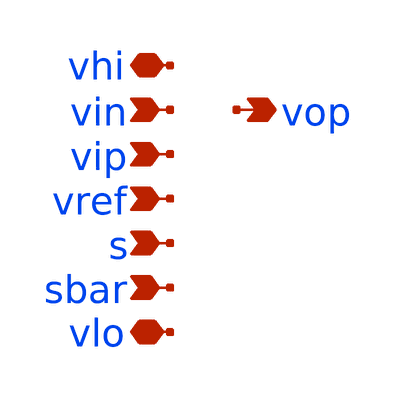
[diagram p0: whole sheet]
** sch_path: xschem/dut_opa_top_pex.sch
**.subckt dut_opa_top_pex vip vin vop vhi vlo vref s sbar
*.ipin vip
*.ipin vin
*.opin vop
*.iopin vhi
*.iopin vlo
*.ipin vref
*.ipin s
*.ipin sbar
**** begin user architecture code

* NGSPICE file created from cmota_1_flat.ext - technology: sky130A

.subckt cmota_gb_rp_gp VHI VLO VREF VIP VIN VOP S SBAR


X0 VOP a_19556_n5512# VHI VHI sky130_fd_pr__pfet_01v8 ad=0p pd=0u as=0p ps=0u w=1e+07u l=300000u
X1 a_19201_n6600# VIN a_18258_n5512# VLO sky130_fd_pr__nfet_01v8_lvt ad=0p pd=0u as=0p ps=0u
+ w=2.5e+06u l=150000u
X2 a_18258_n5512# VIN a_19201_n6600# VLO sky130_fd_pr__nfet_01v8_lvt ad=0p pd=0u as=0p ps=0u
+ w=2.5e+06u l=150000u
X3 VLO VLO VLO VLO sky130_fd_pr__nfet_01v8 ad=0p pd=0u as=0p ps=0u w=1e+07u l=300000u
X4 a_18021_n8012# a_22692_n6680# VLO sky130_fd_pr__res_high_po w=690000u l=5.83e+06u
D0 VLO VIP sky130_fd_pr__diode_pw2nd_05v5 pj=2.64e+06 area=4.347e+11
X5 a_19201_n6600# a_16650_n8544# VLO VLO sky130_fd_pr__nfet_01v8 ad=0p pd=0u as=0p ps=0u w=1e+07u
+ l=2e+06u
X6 VLO a_18021_n8012# VOP VLO sky130_fd_pr__nfet_01v8 ad=0p pd=0u as=0p ps=0u w=1e+07u l=300000u
X7 VHI VLO sky130_fd_pr__cap_mim_m3_1 l=3.1e+07u w=1.3e+07u
X8 VLO a_18021_n8012# a_18021_n8012# VLO sky130_fd_pr__nfet_01v8 ad=0p pd=0u as=0p ps=0u w=1e+07u
+ l=300000u
X9 a_16606_n9004# S a_16650_n8544# VLO sky130_fd_pr__nfet_01v8 ad=0p pd=0u as=0p ps=0u w=2.5e+06u
+ l=150000u
D1 VREF VHI sky130_fd_pr__diode_pd2nw_05v5 pj=3.34e+06 area=6.552e+11
X10 VLO a_16650_n8544# sky130_fd_pr__cap_mim_m3_1 l=2.7e+07u w=5.5e+06u
X11 VLO VLO VLO VLO sky130_fd_pr__nfet_01v8 ad=0p pd=0u as=0p ps=0u w=1e+07u l=300000u
X12 a_19619_n5415# a_19556_n5512# VHI VHI sky130_fd_pr__pfet_01v8 ad=0p pd=0u as=0p ps=0u w=1e+07u
+ l=300000u
X13 VHI a_19556_n5512# a_19619_n5415# VHI sky130_fd_pr__pfet_01v8 ad=0p pd=0u as=0p ps=0u w=1e+07u
+ l=300000u
X14 VHI a_18258_n5512# a_19556_n5512# VHI sky130_fd_pr__pfet_01v8 ad=0p pd=0u as=0p ps=0u w=1e+07u
+ l=300000u
X15 VOP a_19556_n5512# VHI VHI sky130_fd_pr__pfet_01v8 ad=0p pd=0u as=0p ps=0u w=1e+07u l=300000u
X16 a_19556_n5512# VIP a_19201_n6600# VLO sky130_fd_pr__nfet_01v8_lvt ad=0p pd=0u as=0p ps=0u
+ w=2.5e+06u l=150000u
D2 VIP VHI sky130_fd_pr__diode_pd2nw_05v5 pj=3.34e+06 area=6.552e+11
X17 a_18258_n5512# a_19556_n5512# VHI VHI sky130_fd_pr__pfet_01v8 ad=0p pd=0u as=0p ps=0u w=1e+07u
+ l=300000u
X18 a_20327_n5415# a_18258_n5512# VHI VHI sky130_fd_pr__pfet_01v8 ad=0p pd=0u as=0p ps=0u w=1e+07u
+ l=300000u
X19 a_19201_n6600# VIP a_19556_n5512# VLO sky130_fd_pr__nfet_01v8_lvt ad=0p pd=0u as=0p ps=0u
+ w=2.5e+06u l=150000u
X20 VHI a_18258_n5512# a_20327_n5415# VHI sky130_fd_pr__pfet_01v8 ad=0p pd=0u as=0p ps=0u w=1e+07u
+ l=300000u
X21 a_18021_n8012# a_18258_n5512# VHI VHI sky130_fd_pr__pfet_01v8 ad=0p pd=0u as=0p ps=0u w=1e+07u
+ l=300000u
X22 a_18258_n5512# VIN a_19201_n6600# VLO sky130_fd_pr__nfet_01v8_lvt ad=0p pd=0u as=0p ps=0u
+ w=2.5e+06u l=150000u
X23 a_19201_n6600# a_16650_n8544# VLO VLO sky130_fd_pr__nfet_01v8 ad=0p pd=0u as=0p ps=0u w=1e+07u
+ l=2e+06u
X24 VHI a_18258_n5512# a_18021_n8012# VHI sky130_fd_pr__pfet_01v8 ad=0p pd=0u as=0p ps=0u w=1e+07u
+ l=300000u
X25 a_18021_n8012# a_18258_n5512# VHI VHI sky130_fd_pr__pfet_01v8 ad=0p pd=0u as=0p ps=0u w=1e+07u
+ l=300000u
X26 a_19201_n6600# VIN a_18258_n5512# VLO sky130_fd_pr__nfet_01v8_lvt ad=0p pd=0u as=0p ps=0u
+ w=2.5e+06u l=150000u
X27 a_19201_n6600# VIP a_19556_n5512# VLO sky130_fd_pr__nfet_01v8_lvt ad=0p pd=0u as=0p ps=0u
+ w=2.5e+06u l=150000u
X28 VLO a_16650_n8544# a_19201_n6600# VLO sky130_fd_pr__nfet_01v8 ad=0p pd=0u as=0p ps=0u w=1e+07u
+ l=2e+06u
X29 a_16650_n8544# VLO sky130_fd_pr__cap_mim_m3_2 l=2.7e+07u w=5.5e+06u
X30 VLO VHI sky130_fd_pr__cap_mim_m3_2 l=3.1e+07u w=1.3e+07u
X31 VLO VLO VLO VLO sky130_fd_pr__nfet_01v8_lvt ad=0p pd=0u as=0p ps=0u w=2.5e+06u l=150000u
X32 VLO VLO a_19201_n6600# VLO sky130_fd_pr__nfet_01v8_lvt ad=0p pd=0u as=0p ps=0u w=2.5e+06u
+ l=150000u
X33 VLO VLO VLO VLO sky130_fd_pr__nfet_01v8_lvt ad=0p pd=0u as=0p ps=0u w=2.5e+06u l=150000u
X34 VOP a_22692_n6680# sky130_fd_pr__cap_mim_m3_1 l=1.32e+07u w=3.7e+06u
X35 a_19201_n6600# VIN a_18258_n5512# VLO sky130_fd_pr__nfet_01v8_lvt ad=0p pd=0u as=0p ps=0u
+ w=2.5e+06u l=150000u
X36 a_16650_n8544# S a_16606_n9004# VLO sky130_fd_pr__nfet_01v8 ad=0p pd=0u as=0p ps=0u w=2.5e+06u
+ l=150000u
X37 VREF a_16606_n9004# VLO sky130_fd_pr__res_xhigh_po w=350000u l=1.49e+06u
X38 VLO VLO VLO VLO sky130_fd_pr__nfet_01v8 ad=0p pd=0u as=0p ps=0u w=1e+07u l=300000u
X39 VOP a_18021_n8012# VLO VLO sky130_fd_pr__nfet_01v8 ad=0p pd=0u as=0p ps=0u w=1e+07u l=300000u
X40 VHI a_19556_n5512# VOP VHI sky130_fd_pr__pfet_01v8 ad=0p pd=0u as=0p ps=0u w=1e+07u l=300000u
X41 a_19201_n6600# VLO VLO VLO sky130_fd_pr__nfet_01v8_lvt ad=0p pd=0u as=0p ps=0u w=2.5e+06u
+ l=150000u
X42 a_16606_n9004# SBAR VLO VLO sky130_fd_pr__nfet_01v8 ad=0p pd=0u as=0p ps=0u w=2.5e+06u l=150000u
X43 VLO a_18021_n8012# VOP VLO sky130_fd_pr__nfet_01v8 ad=0p pd=0u as=0p ps=0u w=1e+07u l=300000u
X44 a_18258_n5512# a_18258_n5512# VHI VHI sky130_fd_pr__pfet_01v8 ad=0p pd=0u as=0p ps=0u w=1e+07u
+ l=300000u
X45 VOP a_19556_n5512# VHI VHI sky130_fd_pr__pfet_01v8 ad=0p pd=0u as=0p ps=0u w=1e+07u l=300000u
X46 a_18258_n5512# VIN a_19201_n6600# VLO sky130_fd_pr__nfet_01v8_lvt ad=0p pd=0u as=0p ps=0u
+ w=2.5e+06u l=150000u
D3 VLO VIN sky130_fd_pr__diode_pw2nd_05v5 pj=2.64e+06 area=4.347e+11
X47 VHI a_19556_n5512# VOP VHI sky130_fd_pr__pfet_01v8 ad=0p pd=0u as=0p ps=0u w=1e+07u l=300000u
X48 VOP a_19556_n5512# VHI VHI sky130_fd_pr__pfet_01v8 ad=0p pd=0u as=0p ps=0u w=1e+07u l=300000u
X49 a_22692_n6680# VOP sky130_fd_pr__cap_mim_m3_2 l=1.32e+07u w=3.7e+06u
X50 a_18021_n8012# VHI VHI VHI sky130_fd_pr__pfet_01v8 ad=0p pd=0u as=0p ps=0u w=1e+07u l=300000u
X51 VHI a_18258_n5512# a_18021_n8012# VHI sky130_fd_pr__pfet_01v8 ad=0p pd=0u as=0p ps=0u w=1e+07u
+ l=300000u
X52 VHI a_19556_n5512# a_18258_n5512# VHI sky130_fd_pr__pfet_01v8 ad=0p pd=0u as=0p ps=0u w=1e+07u
+ l=300000u
X53 a_19556_n5512# a_19556_n5512# VHI VHI sky130_fd_pr__pfet_01v8 ad=0p pd=0u as=0p ps=0u w=1e+07u
+ l=300000u
D4 VIN VHI sky130_fd_pr__diode_pd2nw_05v5 pj=3.34e+06 area=6.552e+11
X54 VHI a_18258_n5512# a_18021_n8012# VHI sky130_fd_pr__pfet_01v8 ad=0p pd=0u as=0p ps=0u w=1e+07u
+ l=300000u
X55 VHI a_19556_n5512# a_19556_n5512# VHI sky130_fd_pr__pfet_01v8 ad=0p pd=0u as=0p ps=0u w=1e+07u
+ l=300000u
X56 a_19556_n5512# VIP a_19201_n6600# VLO sky130_fd_pr__nfet_01v8_lvt ad=0p pd=0u as=0p ps=0u
+ w=2.5e+06u l=150000u
X57 a_19556_n5512# VIP a_19201_n6600# VLO sky130_fd_pr__nfet_01v8_lvt ad=0p pd=0u as=0p ps=0u
+ w=2.5e+06u l=150000u
D5 VLO VREF sky130_fd_pr__diode_pw2nd_05v5 pj=2.64e+06 area=4.347e+11
X58 a_19201_n6600# VIP a_19556_n5512# VLO sky130_fd_pr__nfet_01v8_lvt ad=0p pd=0u as=0p ps=0u
+ w=2.5e+06u l=150000u
X59 a_18021_n8012# a_18021_n8012# VLO VLO sky130_fd_pr__nfet_01v8 ad=0p pd=0u as=0p ps=0u w=1e+07u
+ l=300000u
X60 a_18258_n5512# VIN a_19201_n6600# VLO sky130_fd_pr__nfet_01v8_lvt ad=0p pd=0u as=0p ps=0u
+ w=2.5e+06u l=150000u
X61 VLO SBAR a_16606_n9004# VLO sky130_fd_pr__nfet_01v8 ad=0p pd=0u as=0p ps=0u w=2.5e+06u l=150000u
X62 VHI a_19556_n5512# VOP VHI sky130_fd_pr__pfet_01v8 ad=0p pd=0u as=0p ps=0u w=1e+07u l=300000u
X63 VLO a_18021_n8012# a_18021_n8012# VLO sky130_fd_pr__nfet_01v8 ad=0p pd=0u as=0p ps=0u w=1e+07u
+ l=300000u
X64 a_19201_n6600# VIN a_18258_n5512# VLO sky130_fd_pr__nfet_01v8_lvt ad=0p pd=0u as=0p ps=0u
+ w=2.5e+06u l=150000u
X65 a_19201_n6600# VIP a_19556_n5512# VLO sky130_fd_pr__nfet_01v8_lvt ad=0p pd=0u as=0p ps=0u
+ w=2.5e+06u l=150000u
X66 VOP a_18021_n8012# VLO VLO sky130_fd_pr__nfet_01v8 ad=0p pd=0u as=0p ps=0u w=1e+07u l=300000u
X67 VHI a_18258_n5512# a_18258_n5512# VHI sky130_fd_pr__pfet_01v8 ad=0p pd=0u as=0p ps=0u w=1e+07u
+ l=300000u
X68 a_18258_n5512# a_18258_n5512# VHI VHI sky130_fd_pr__pfet_01v8 ad=0p pd=0u as=0p ps=0u w=1e+07u
+ l=300000u
X69 a_19556_n5512# a_19556_n5512# VHI VHI sky130_fd_pr__pfet_01v8 ad=0p pd=0u as=0p ps=0u w=1e+07u
+ l=300000u
X70 a_18021_n8012# a_18021_n8012# VLO VLO sky130_fd_pr__nfet_01v8 ad=0p pd=0u as=0p ps=0u w=1e+07u
+ l=300000u
X71 a_19556_n5512# VIP a_19201_n6600# VLO sky130_fd_pr__nfet_01v8_lvt ad=0p pd=0u as=0p ps=0u
+ w=2.5e+06u l=150000u
X72 VLO a_16650_n8544# a_19201_n6600# VLO sky130_fd_pr__nfet_01v8 ad=0p pd=0u as=0p ps=0u w=1e+07u
+ l=2e+06u
X73 a_18021_n8012# a_18258_n5512# VHI VHI sky130_fd_pr__pfet_01v8 ad=0p pd=0u as=0p ps=0u w=1e+07u
+ l=300000u
X74 VHI a_18258_n5512# a_18021_n8012# VHI sky130_fd_pr__pfet_01v8 ad=0p pd=0u as=0p ps=0u w=1e+07u
+ l=300000u
X75 VHI a_18258_n5512# a_18258_n5512# VHI sky130_fd_pr__pfet_01v8 ad=0p pd=0u as=0p ps=0u w=1e+07u
+ l=300000u
X76 a_19556_n5512# a_18258_n5512# VHI VHI sky130_fd_pr__pfet_01v8 ad=0p pd=0u as=0p ps=0u w=1e+07u
+ l=300000u
X77 VHI a_19556_n5512# a_19556_n5512# VHI sky130_fd_pr__pfet_01v8 ad=0p pd=0u as=0p ps=0u w=1e+07u
+ l=300000u
X78 VHI VHI VOP VHI sky130_fd_pr__pfet_01v8 ad=0p pd=0u as=0p ps=0u w=1e+07u l=300000u
X79 VLO VLO VLO VLO sky130_fd_pr__nfet_01v8 ad=0p pd=0u as=0p ps=0u w=1e+07u l=300000u
C0 a_19556_n5512# a_19201_n6600# 6.02fF
C1 VHI a_16650_n8544# 4.87fF
C2 a_22692_n6680# VHI 3.27fF
C3 VIP VIN 8.58fF
C4 a_18258_n5512# a_19201_n6600# 6.05fF
C5 a_20327_n5415# VHI 4.36fF
C6 a_18021_n8012# VHI 17.95fF
C7 S SBAR 4.58fF
C8 a_16650_n8544# a_19201_n6600# 2.51fF
C9 VREF SBAR 9.93fF
C10 VIP VOP 7.94fF
C11 VOP VHI 18.78fF
C12 a_22692_n6680# VOP 9.58fF
C13 a_19556_n5512# VHI 17.03fF
C14 VHI a_19619_n5415# 4.36fF
C15 a_18258_n5512# VHI 17.11fF
C16 VREF VIN 3.09fF
C17 a_22692_n6680# VLO 2.59fF $ **FLOATING
C18 VREF VLO 79.79fF $ **FLOATING
C19 SBAR VLO 70.93fF $ **FLOATING
C20 a_16650_n8544# VLO 50.04fF $ **FLOATING
C21 S VLO 75.15fF $ **FLOATING
C22 a_19201_n6600# VLO 6.13fF $ **FLOATING
C23 VIP VLO 74.57fF $ **FLOATING
C24 VIN VLO 84.21fF $ **FLOATING
C25 VOP VLO 86.69fF $ **FLOATING
C26 a_18021_n8012# VLO 14.03fF $ **FLOATING
C27 VHI VLO 192.78fF $ **FLOATING


.ends

XDUT vhi vlo vref vip vin vop s sbar cmota_gb_rp_gp


**** end user architecture code
**.ends
.end
